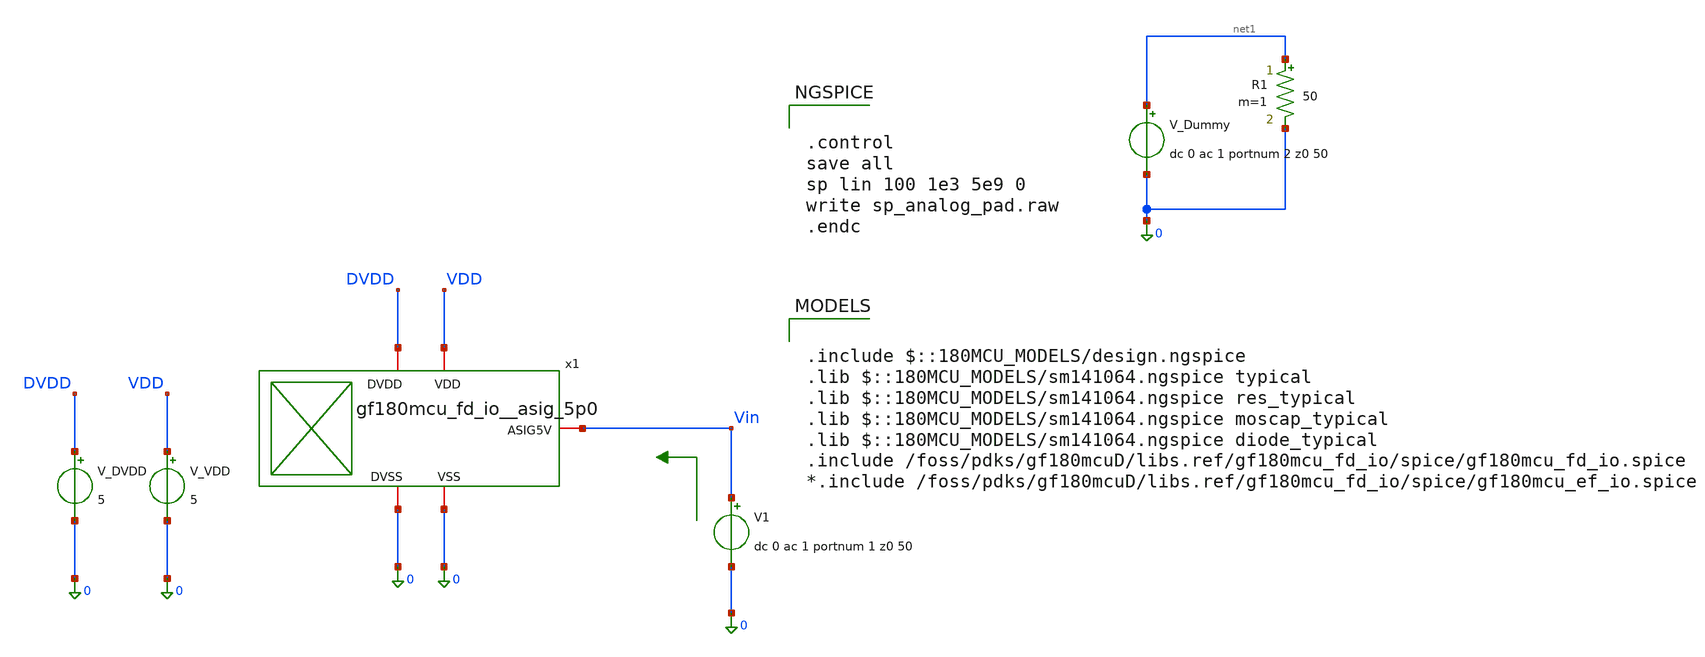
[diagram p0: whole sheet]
** sch_path: Pads_Simulation/schematic_sp.sch
**.subckt schematic_sp
x1 Vin DVDD 0 VDD 0 gf180mcu_fd_io__asig_5p0
V1 Vin 0 dc 0 ac 1 portnum 1 z0 50
V_VDD VDD 0 5
V_DVDD DVDD 0 5
V_Dummy net1 0 dc 0 ac 1 portnum 2 z0 50
R1 net1 0 50 m=1
**** begin user architecture code


.control
save all
sp lin 100 1e3 5e9 0
write sp_analog_pad.raw
.endc



.include $::180MCU_MODELS/design.ngspice
.lib $::180MCU_MODELS/sm141064.ngspice typical
.lib $::180MCU_MODELS/sm141064.ngspice res_typical
.lib $::180MCU_MODELS/sm141064.ngspice moscap_typical
.lib $::180MCU_MODELS/sm141064.ngspice diode_typical
.include /foss/pdks/gf180mcuD/libs.ref/gf180mcu_fd_io/spice/gf180mcu_fd_io.spice
*.include /foss/pdks/gf180mcuD/libs.ref/gf180mcu_fd_io/spice/gf180mcu_ef_io.spice

**** end user architecture code
**.ends
.end
